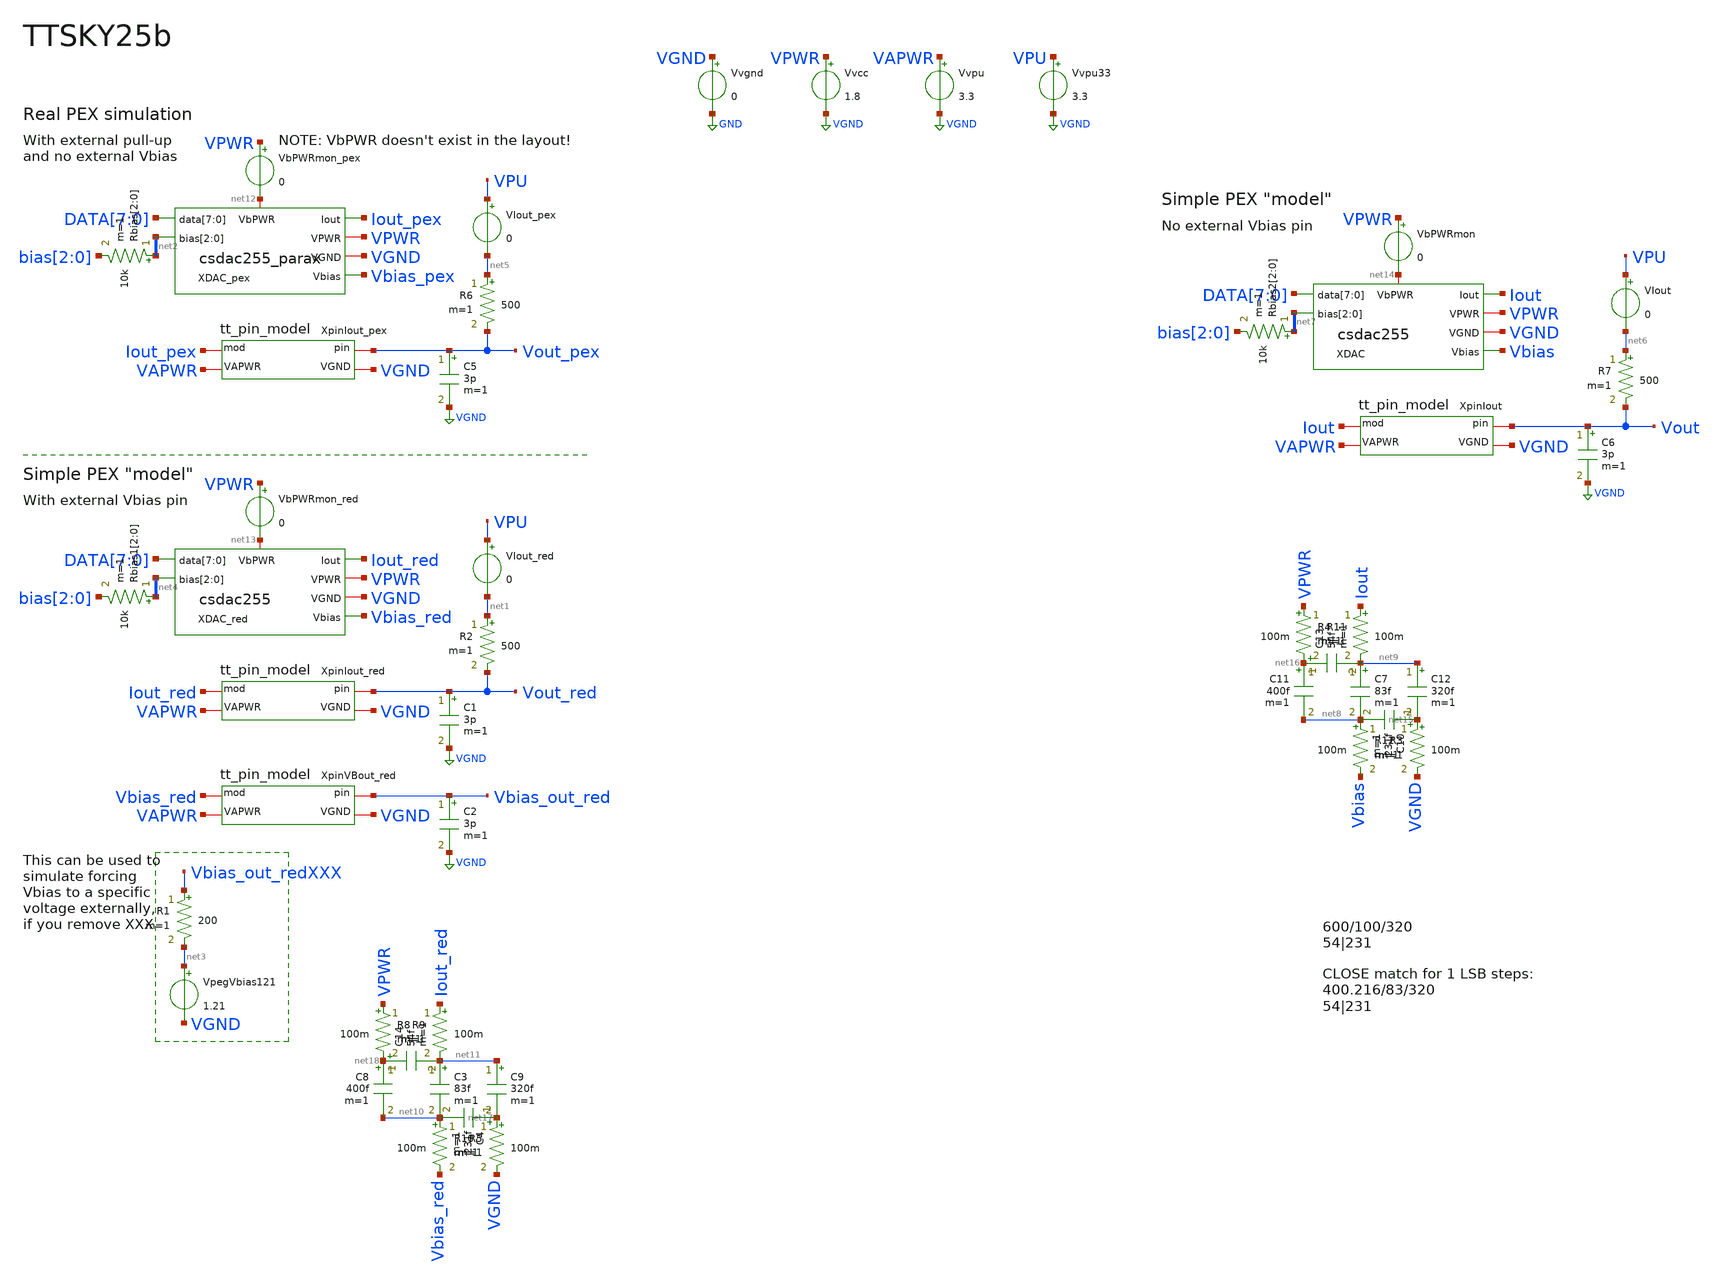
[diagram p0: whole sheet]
** sch_path: xschem/tb_csdac255.sch
**.subckt tb_csdac255
Vvcc VPWR VGND 1.8
Vvpu VAPWR VGND 3.3
Vvgnd VGND GND 0
XDAC_pex DATA[7] DATA[6] DATA[5] DATA[4] DATA[3] DATA[2] DATA[1] DATA[0] Iout_pex VPWR VGND
+ Vbias_pex net2[2] net2[1] net2[0] net12 csdac255_parax
XpinIout_red VGND VAPWR Iout_red Vout_red tt_pin_model
R2 net1 Vout_red 500 m=1
VIout_red VPU net1 0
C1 Vout_red VGND 3p m=1
Rbias[2] net2[2] bias[2] 10k m=1
Rbias[1] net2[1] bias[1] 10k m=1
Rbias[0] net2[0] bias[0] 10k m=1
VbPWRmon_pex VPWR net12 0
VpegVbias121 net3 VGND 1.21
R1 Vbias_out_redXXX net3 200 m=1
XpinVBout_red VGND VAPWR Vbias_red Vbias_out_red tt_pin_model
C2 Vbias_out_red VGND 3p m=1
Vvpu33 VPU VGND 3.3
XDAC_red DATA[7] DATA[6] DATA[5] DATA[4] DATA[3] DATA[2] DATA[1] DATA[0] Iout_red VPWR VGND
+ Vbias_red net4[2] net4[1] net4[0] net13 csdac255
Rbias1[2] net4[2] bias[2] 10k m=1
Rbias1[1] net4[1] bias[1] 10k m=1
Rbias1[0] net4[0] bias[0] 10k m=1
VbPWRmon_red VPWR net13 0
XpinIout_pex VGND VAPWR Iout_pex Vout_pex tt_pin_model
R6 net5 Vout_pex 500 m=1
VIout_pex VPU net5 0
C5 Vout_pex VGND 3p m=1
XpinIout VGND VAPWR Iout Vout tt_pin_model
R7 net6 Vout 500 m=1
VIout VPU net6 0
C6 Vout VGND 3p m=1
XDAC DATA[7] DATA[6] DATA[5] DATA[4] DATA[3] DATA[2] DATA[1] DATA[0] Iout VPWR VGND Vbias net7[2]
+ net7[1] net7[0] net14 csdac255
Rbias2[2] net7[2] bias[2] 10k m=1
Rbias2[1] net7[1] bias[1] 10k m=1
Rbias2[0] net7[0] bias[0] 10k m=1
VbPWRmon VPWR net14 0
C7 net9 net8 83f m=1
C10 net15 net8 231f m=1
C11 net16 net8 400f m=1
C12 net9 net15 320f m=1
C13 net16 net9 54f m=1
C3 net11 net10 83f m=1
C4 net17 net10 231f m=1
C8 net18 net10 400f m=1
C9 net11 net17 320f m=1
C14 net18 net11 54f m=1
R3 net15 VGND 100m m=1
R4 VPWR net16 100m m=1
R5 net17 VGND 100m m=1
R8 VPWR net18 100m m=1
R9 Iout_red net11 100m m=1
R10 net10 Vbias_red 100m m=1
R11 Iout net9 100m m=1
R12 net8 Vbias 100m m=1
**** begin user architecture code




* Set Vbias level (negative logic, so 0=ON, 1.8=OFF):
.param bias2=1.8
.param bias1=1.8
.param bias0=1.8
Vvbias2 bias[2] GND {bias2}
Vvbias1 bias[1] GND {bias1}
Vvbias0 bias[0] GND {bias0}

*NOTE: Possible ngspice bug with .IF(), so it's commented out here:
*.param singlebits=0
*.IF (singlebits == 1)
* Mode to just test each binary-weighted level:
*Vxp0 DATA[0]  GND pulse 0v 1.8v 1u 1n 1n 1u 10u
*Vxp1 DATA[1]  GND pulse 0v 1.8v 2u 1n 1n 1u 10u
*Vxp2 DATA[2]  GND pulse 0v 1.8v 3u 1n 1n 1u 10u
*Vxp3 DATA[3]  GND pulse 0v 1.8v 4u 1n 1n 1u 10u
*Vxp4 DATA[4]  GND pulse 0v 1.8v 5u 1n 1n 1u 10u
*Vxp5 DATA[5]  GND pulse 0v 1.8v 6u 1n 1n 1u 10u
*Vxp6 DATA[6]  GND pulse 0v 1.8v 7u 1n 1n 1u 10u
*Vxp7 DATA[7]  GND pulse 0v 1.8v 8u 1n 1n 1u 10u
*.ELSEIF (singlebits == 0)
** Mode to test full 0..255 range:
*Vxp0 DATA[0]  GND pulse 1.8v 0v 0n 1n 1n 39n 80n
*Vxp1 DATA[1]  GND pulse 1.8v 0v 0n 1n 1n 79n 160n
*Vxp2 DATA[2]  GND pulse 1.8v 0v 0n 1n 1n 159n 320n
*Vxp3 DATA[3]  GND pulse 1.8v 0v 0n 1n 1n 319n 640n
*Vxp4 DATA[4]  GND pulse 1.8v 0v 0n 1n 1n 639n 1280n
*Vxp5 DATA[5]  GND pulse 1.8v 0v 0n 1n 1n 1279n 2560n
*Vxp6 DATA[6]  GND pulse 1.8v 0v 0n 1n 1n 2559n 5120n
*Vxp7 DATA[7]  GND pulse 1.8v 0v 0n 1n 1n 5119n 10240n
* INVERTED test of full range (255..0):
Vxp0 DATA[0]  GND pulse 0v 1.8v 0n 1n 1n 39n 80n
Vxp1 DATA[1]  GND pulse 0v 1.8v 0n 1n 1n 79n 160n
Vxp2 DATA[2]  GND pulse 0v 1.8v 0n 1n 1n 159n 320n
Vxp3 DATA[3]  GND pulse 0v 1.8v 0n 1n 1n 319n 640n
Vxp4 DATA[4]  GND pulse 0v 1.8v 0n 1n 1n 639n 1280n
Vxp5 DATA[5]  GND pulse 0v 1.8v 0n 1n 1n 1279n 2560n
Vxp6 DATA[6]  GND pulse 0v 1.8v 0n 1n 1n 2559n 5120n
Vxp7 DATA[7]  GND pulse 0v 1.8v 0n 1n 1n 5119n 10240n
*.endif

*.options savecurrents

* 100G-ohm shunt from all nodes to GND:
.option rshunt = 1.0e11

*.options method=trap xmu=0.495
*.options method=gear

.control
	* Start with all bias[*] switches at 0V (ENb), so highest Vbias (max current sink):
	let biaslevel=7
	foreach bv2 0 1.8
		foreach bv1 0 1.8
			foreach bv0 0 1.8
				alterparam bias2 = $bv2
				alterparam bias1 = $bv1
				alterparam bias0 = $bv0
				reset
				echo Bias level $&biaslevel = $bv2 $bv1 $bv0
				save
				+ data[0] data[1] data[2] data[3] data[4] data[5] data[6] data[7]
				+ bias[0] bias[1] bias[2]
				+ vbias
				+ vbias_red vbias_out_red
				+ vbias_pex
				+ i(viout_pex)
				+ i(viout_red)
				+ i(viout)
				+ i(vvpu33)
				+ vout
				+ vout_pex
				+ vout_red
				+ i(vvcc)
				+ i(vvpu)
				+ i(vvgnd)
				+ i(vbpwrmon)
				+ i(vbpwrmon_red)
				+ i(vbpwrmon_pex)
				+ XDAC.vbias_in
				+ XDAC_red.vbias_in
				+ XDAC.THERMO_ROWn[0] XDAC.THERMO_ROWn[1] XDAC.THERMO_ROWn[2] XDAC.THERMO_ROWn[3] XDAC.THERMO_ROWn[4] XDAC.THERMO_ROWn[5] XDAC.THERMO_ROWn[6] XDAC.THERMO_ROWn[7] XDAC.THERMO_ROWn[8] XDAC.THERMO_ROWn[9] XDAC.THERMO_ROWn[10] XDAC.THERMO_ROWn[11] XDAC.THERMO_ROWn[12] XDAC.THERMO_ROWn[13] XDAC.THERMO_ROWn[14]
				+ XDAC.THERMO_COLn[0] XDAC.THERMO_COLn[1] XDAC.THERMO_COLn[2] XDAC.THERMO_COLn[3] XDAC.THERMO_COLn[4] XDAC.THERMO_COLn[5] XDAC.THERMO_COLn[6] XDAC.THERMO_COLn[7] XDAC.THERMO_COLn[8] XDAC.THERMO_COLn[9] XDAC.THERMO_COLn[10] XDAC.THERMO_COLn[11] XDAC.THERMO_COLn[12] XDAC.THERMO_COLn[13] XDAC.THERMO_COLn[14]
				+ XDAC.XThR.TA1 XDAC.XThR.TA2 XDAC.XThR.TA3 XDAC.XThR.TAN XDAC.XThR.TAN2 XDAC.XThR.TB1 XDAC.XThR.TB2 XDAC.XThR.TB3 XDAC.XThR.TB4 XDAC.XThR.TB5 XDAC.XThR.TB6 XDAC.XThR.TB7 XDAC.XThR.TBN
				+ XDAC.XThC.TA1 XDAC.XThC.TA2 XDAC.XThC.TA3 XDAC.XThC.TAN XDAC.XThC.TAN2 XDAC.XThC.TB1 XDAC.XThC.TB2 XDAC.XThC.TB3 XDAC.XThC.TB4 XDAC.XThC.TB5 XDAC.XThC.TB6 XDAC.XThC.TB7 XDAC.XThC.TBN
				+ XDAC_red.THERMO_ROWn[0] XDAC_red.THERMO_ROWn[1] XDAC_red.THERMO_ROWn[2] XDAC_red.THERMO_ROWn[3] XDAC_red.THERMO_ROWn[4] XDAC_red.THERMO_ROWn[5] XDAC_red.THERMO_ROWn[6] XDAC_red.THERMO_ROWn[7] XDAC_red.THERMO_ROWn[8] XDAC_red.THERMO_ROWn[9] XDAC_red.THERMO_ROWn[10] XDAC_red.THERMO_ROWn[11] XDAC_red.THERMO_ROWn[12] XDAC_red.THERMO_ROWn[13] XDAC_red.THERMO_ROWn[14]
				+ XDAC_red.THERMO_COLn[0] XDAC_red.THERMO_COLn[1] XDAC_red.THERMO_COLn[2] XDAC_red.THERMO_COLn[3] XDAC_red.THERMO_COLn[4] XDAC_red.THERMO_COLn[5] XDAC_red.THERMO_COLn[6] XDAC_red.THERMO_COLn[7] XDAC_red.THERMO_COLn[8] XDAC_red.THERMO_COLn[9] XDAC_red.THERMO_COLn[10] XDAC_red.THERMO_COLn[11] XDAC_red.THERMO_COLn[12] XDAC_red.THERMO_COLn[13] XDAC_red.THERMO_COLn[14]
				+ XDAC_red.XThR.TA1 XDAC_red.XThR.TA2 XDAC_red.XThR.TA3 XDAC_red.XThR.TAN XDAC_red.XThR.TAN2 XDAC_red.XThR.TB1 XDAC_red.XThR.TB2 XDAC_red.XThR.TB3 XDAC_red.XThR.TB4 XDAC_red.XThR.TB5 XDAC_red.XThR.TB6 XDAC_red.XThR.TB7 XDAC_red.XThR.TBN
				+ XDAC_red.XThC.TA1 XDAC_red.XThC.TA2 XDAC_red.XThC.TA3 XDAC_red.XThC.TAN XDAC_red.XThC.TAN2 XDAC_red.XThC.TB1 XDAC_red.XThC.TB2 XDAC_red.XThC.TB3 XDAC_red.XThC.TB4 XDAC_red.XThC.TB5 XDAC_red.XThC.TB6 XDAC_red.XThC.TB7 XDAC_red.XThC.TBN				+ XDAC_PEX.XThR.Tn[0] XDAC_PEX.XThR.Tn[1] XDAC_PEX.XThR.Tn[2] XDAC_PEX.XThR.Tn[3] XDAC_PEX.XThR.Tn[4] XDAC_PEX.XThR.Tn[5] XDAC_PEX.XThR.Tn[6] XDAC_PEX.XThR.Tn[7] XDAC_PEX.XThR.Tn[8] XDAC_PEX.XThR.Tn[9] XDAC_PEX.XThR.Tn[10] XDAC_PEX.XThR.Tn[11] XDAC_PEX.XThR.Tn[12] XDAC_PEX.XThR.Tn[13] XDAC_PEX.XThR.Tn[14]
				+ XDAC_PEX.XThC.Tn[0] XDAC_PEX.XThC.Tn[1] XDAC_PEX.XThC.Tn[2] XDAC_PEX.XThC.Tn[3] XDAC_PEX.XThC.Tn[4] XDAC_PEX.XThC.Tn[5] XDAC_PEX.XThC.Tn[6] XDAC_PEX.XThC.Tn[7] XDAC_PEX.XThC.Tn[8] XDAC_PEX.XThC.Tn[9] XDAC_PEX.XThC.Tn[10] XDAC_PEX.XThC.Tn[11] XDAC_PEX.XThC.Tn[12] XDAC_PEX.XThC.Tn[13] XDAC_PEX.XThC.Tn[14]
				+ XDAC_PEX.XThR.TA1 XDAC_PEX.XThR.TA2 XDAC_PEX.XThR.TA3 XDAC_PEX.XThR.TAN XDAC_PEX.XThR.TAN2 XDAC_PEX.XThR.TB1 XDAC_PEX.XThR.TB2 XDAC_PEX.XThR.TB3 XDAC_PEX.XThR.TB4 XDAC_PEX.XThR.TB5 XDAC_PEX.XThR.TB6 XDAC_PEX.XThR.TB7 XDAC_PEX.XThR.TBN
				+ XDAC_PEX.XThC.TA1 XDAC_PEX.XThC.TA2 XDAC_PEX.XThC.TA3 XDAC_PEX.XThC.TAN XDAC_PEX.XThC.TAN2 XDAC_PEX.XThC.TB1 XDAC_PEX.XThC.TB2 XDAC_PEX.XThC.TB3 XDAC_PEX.XThC.TB4 XDAC_PEX.XThC.TB5 XDAC_PEX.XThC.TB6 XDAC_PEX.XThC.TB7 XDAC_PEX.XThC.TBN
				tran 1n 22u uic
				write tb_csdac255_vbias085_x4.raw
				*plot vout vbias i(viout)*1000
				set appendwrite
				reset
				let biaslevel = biaslevel - 1
			end
		end
	end
.endc




.lib /home/anton/asic/ciel/sky130A/libs.tech/combined/sky130.lib.spice tt
.include $::SKYWATER_STDCELLS/sky130_fd_sc_hd.spice

**** end user architecture code
**.ends
.GLOBAL GND
.GLOBAL VGND
.end
